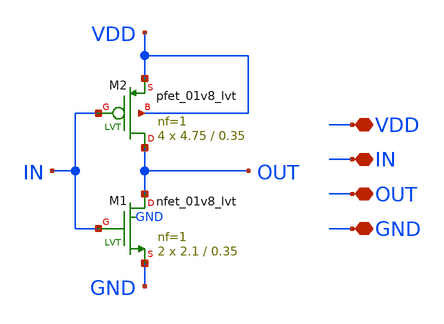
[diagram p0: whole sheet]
** sch_path: LVT/inv_LVT/inv_LVT.sch
**.subckt inv_LVT VDD IN OUT GND
*.iopin VDD
*.iopin IN
*.iopin OUT
*.iopin GND
XM1 OUT IN GND GND sky130_fd_pr__nfet_01v8_lvt L=0.35 W=2.1 nf=1 ad='int((nf+1)/2) * W/nf * 0.29' as='int((nf+2)/2) * W/nf * 0.29'
+ pd='2*int((nf+1)/2) * (W/nf + 0.29)' ps='2*int((nf+2)/2) * (W/nf + 0.29)' nrd='0.29 / W' nrs='0.29 / W'
+ sa=0 sb=0 sd=0 mult=2 m=2
XM2 OUT IN VDD VDD sky130_fd_pr__pfet_01v8_lvt L=0.35 W=4.75 nf=1 ad='int((nf+1)/2) * W/nf * 0.29' as='int((nf+2)/2) * W/nf * 0.29'
+ pd='2*int((nf+1)/2) * (W/nf + 0.29)' ps='2*int((nf+2)/2) * (W/nf + 0.29)' nrd='0.29 / W' nrs='0.29 / W'
+ sa=0 sb=0 sd=0 mult=4 m=4
**.ends
.end
